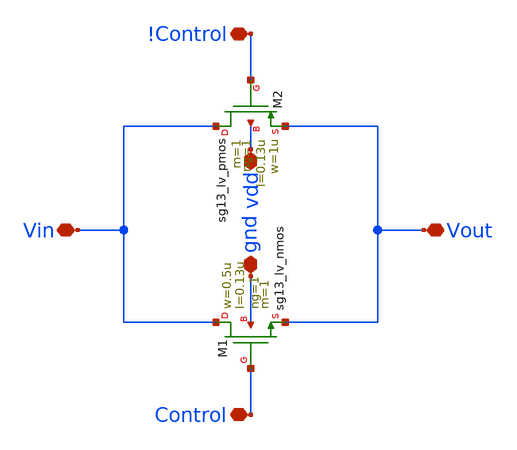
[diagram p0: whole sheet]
** sch_path: xschem/CMOS_transmission_gate.sch
**.subckt CMOS_transmission_gate Vout Vin !Control Control gnd vdd
*.iopin Vout
*.iopin Vin
*.iopin !Control
*.iopin Control
*.iopin gnd
*.iopin vdd
XM1 Vin Control Vout gnd sg13_lv_nmos w=0.5u l=0.13u ng=1 m=1 mm_ok=1
XM2 Vin !Control Vout vdd sg13_lv_pmos w=1u l=0.13u ng=1 m=1 mm_ok=1
**.ends
.end
